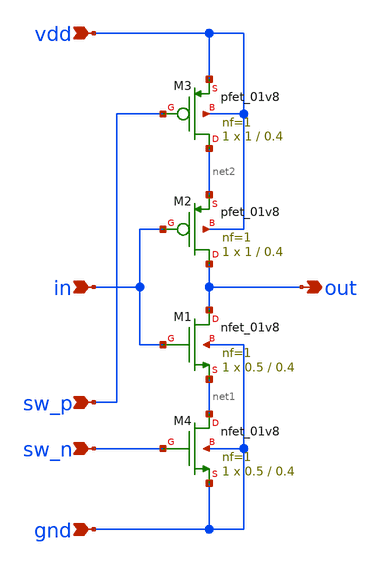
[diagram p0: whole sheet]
** sch_path: xsch/cc_inv_dt05_long.sch
**.subckt cc_inv_dt05_long in vdd gnd out sw_n sw_p
*.ipin in
*.ipin vdd
*.ipin gnd
*.opin out
*.ipin sw_n
*.ipin sw_p
XM1 out in net1 gnd sky130_fd_pr__nfet_01v8 L=0.4 W=0.5 nf=1 ad='int((nf+1)/2) * W/nf * 0.29' as='int((nf+2)/2) * W/nf * 0.29'
+ pd='2*int((nf+1)/2) * (W/nf + 0.29)' ps='2*int((nf+2)/2) * (W/nf + 0.29)' nrd='0.29 / W' nrs='0.29 / W'
+ sa=0 sb=0 sd=0 mult=1 m=1
XM2 out in net2 vdd sky130_fd_pr__pfet_01v8 L=0.4 W=1 nf=1 ad='int((nf+1)/2) * W/nf * 0.29' as='int((nf+2)/2) * W/nf * 0.29'
+ pd='2*int((nf+1)/2) * (W/nf + 0.29)' ps='2*int((nf+2)/2) * (W/nf + 0.29)' nrd='0.29 / W' nrs='0.29 / W'
+ sa=0 sb=0 sd=0 mult=1 m=1
XM3 net2 sw_p vdd vdd sky130_fd_pr__pfet_01v8 L=0.4 W=1 nf=1 ad='int((nf+1)/2) * W/nf * 0.29' as='int((nf+2)/2) * W/nf * 0.29'
+ pd='2*int((nf+1)/2) * (W/nf + 0.29)' ps='2*int((nf+2)/2) * (W/nf + 0.29)' nrd='0.29 / W' nrs='0.29 / W'
+ sa=0 sb=0 sd=0 mult=1 m=1
XM4 net1 sw_n gnd gnd sky130_fd_pr__nfet_01v8 L=0.4 W=0.5 nf=1 ad='int((nf+1)/2) * W/nf * 0.29' as='int((nf+2)/2) * W/nf * 0.29'
+ pd='2*int((nf+1)/2) * (W/nf + 0.29)' ps='2*int((nf+2)/2) * (W/nf + 0.29)' nrd='0.29 / W' nrs='0.29 / W'
+ sa=0 sb=0 sd=0 mult=1 m=1
**.ends
.end
